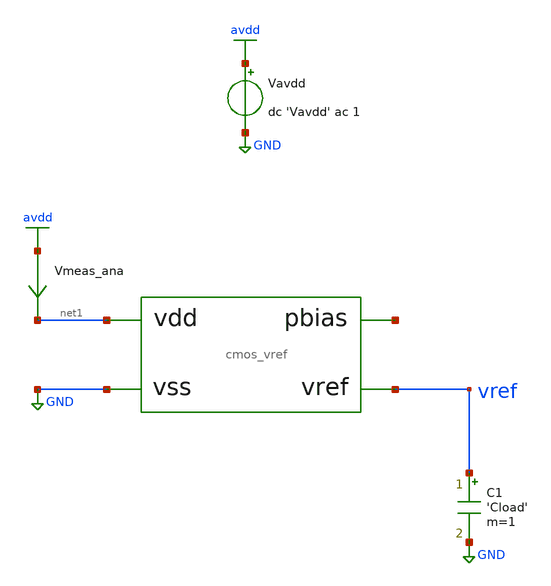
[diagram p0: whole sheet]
** sch_path: tb/cmos_vref/tb_vref_psrr.sch
**.subckt tb_vref_psrr
Vavdd avdd GND dc 'Vavdd' ac 1
C1 vref GND 'Cload' m=1
Vmeas_ana avdd net1 0
.save i(vmeas_ana)
X1 vref net1 GND net2 cmos_vref
**** begin user architecture code


.lib 'models_dir'/cornerMOShv.lib 'mos_corner'
.lib 'models_dir'/cornerMOSlv.lib 'mos_corner'
.lib 'models_dir'/cornerCAP.lib cap_typ
.option TEMP='temperature'
.option warn=1
.control
save vref
ac dec 20 'frequency_start' 'frequency_stop'
set wr_singlescale
wrdata 'simpath'/'filename'_'N'.data vdb(vref)
quit
.endc


**** end user architecture code
**.ends
.GLOBAL avdd
.GLOBAL GND
.end
